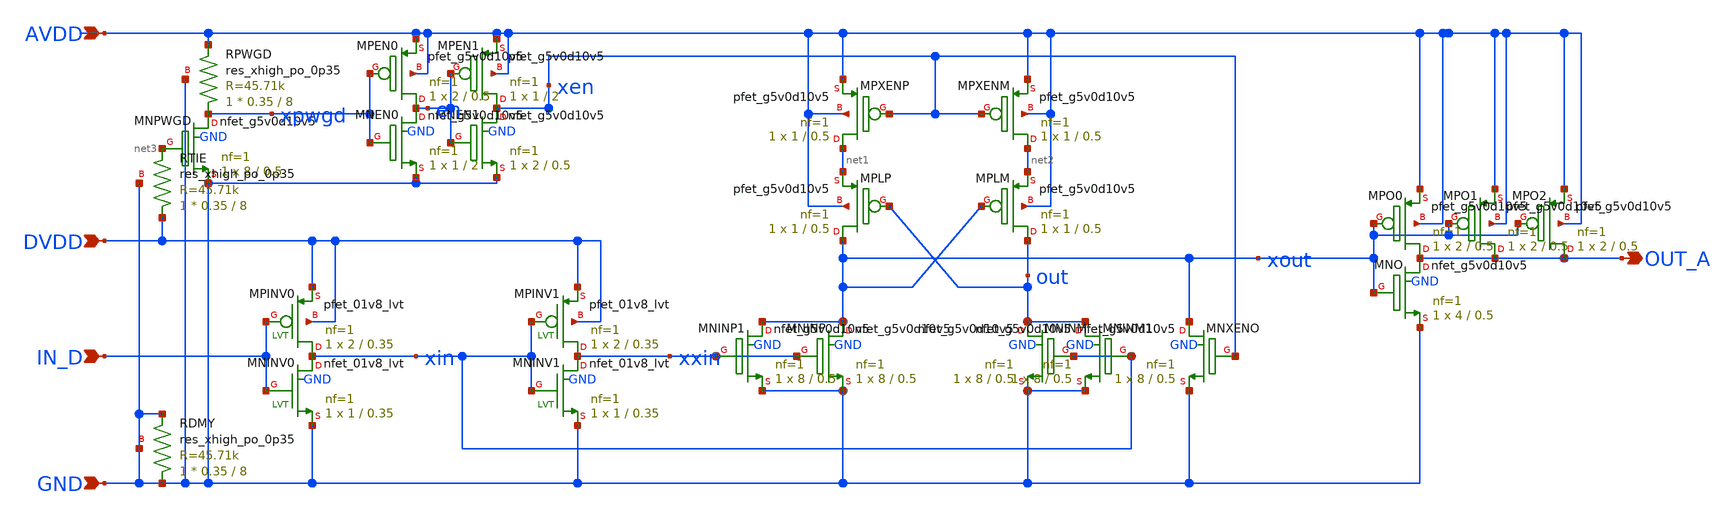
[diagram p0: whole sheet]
** sch_path: design/schematic/LVSHFTL2H_v1.sch
**.subckt LVSHFTL2H_v1 OUT_A AVDD DVDD GND IN_D
*.opin OUT_A
*.ipin AVDD
*.ipin DVDD
*.ipin GND
*.ipin IN_D
XMNINP xout xxin GND GND sky130_fd_pr__nfet_g5v0d10v5 L=0.5 W=8 nf=1 ad='int((nf+1)/2) * W/nf * 0.29'
+ as='int((nf+2)/2) * W/nf * 0.29' pd='2*int((nf+1)/2) * (W/nf + 0.29)' ps='2*int((nf+2)/2) * (W/nf + 0.29)'
+ nrd='0.29 / W' nrs='0.29 / W' sa=0 sb=0 sd=0 mult=1 m=1
XMNINM out xin GND GND sky130_fd_pr__nfet_g5v0d10v5 L=0.5 W=8 nf=1 ad='int((nf+1)/2) * W/nf * 0.29' as='int((nf+2)/2) * W/nf * 0.29'
+ pd='2*int((nf+1)/2) * (W/nf + 0.29)' ps='2*int((nf+2)/2) * (W/nf + 0.29)' nrd='0.29 / W' nrs='0.29 / W'
+ sa=0 sb=0 sd=0 mult=1 m=1
XMPLM out xout net2 AVDD sky130_fd_pr__pfet_g5v0d10v5 L=0.5 W=1 nf=1 ad='int((1 + 1)/2) * 1 / 1 * 0.29'
+ as='int((1 + 2)/2) * 1 / 1 * 0.29' pd='2*int((1 + 1)/2) * (1 / 1 + 0.29)' ps='2*int((1 + 2)/2) * (1 / 1 + 0.29)'
+ nrd='0.29 / 1 ' nrs='0.29 / 1 ' sa=0 sb=0 sd=0 mult=1 m=1
XMPLP xout out net1 AVDD sky130_fd_pr__pfet_g5v0d10v5 L=0.5 W=1 nf=1 ad='int((1 + 1)/2) * 1 / 1 * 0.29'
+ as='int((1 + 2)/2) * 1 / 1 * 0.29' pd='2*int((1 + 1)/2) * (1 / 1 + 0.29)' ps='2*int((1 + 2)/2) * (1 / 1 + 0.29)'
+ nrd='0.29 / 1 ' nrs='0.29 / 1 ' sa=0 sb=0 sd=0 mult=1 m=1
XMPXENM net2 xen AVDD AVDD sky130_fd_pr__pfet_g5v0d10v5 L=0.5 W=1 nf=1 ad='int((1 + 1)/2) * 1 / 1 * 0.29'
+ as='int((1 + 2)/2) * 1 / 1 * 0.29' pd='2*int((1 + 1)/2) * (1 / 1 + 0.29)' ps='2*int((1 + 2)/2) * (1 / 1 + 0.29)'
+ nrd='0.29 / 1 ' nrs='0.29 / 1 ' sa=0 sb=0 sd=0 mult=1 m=1
XMPXENP net1 xen AVDD AVDD sky130_fd_pr__pfet_g5v0d10v5 L=0.5 W=1 nf=1 ad='int((1 + 1)/2) * 1 / 1 * 0.29'
+ as='int((1 + 2)/2) * 1 / 1 * 0.29' pd='2*int((1 + 1)/2) * (1 / 1 + 0.29)' ps='2*int((1 + 2)/2) * (1 / 1 + 0.29)'
+ nrd='0.29 / 1 ' nrs='0.29 / 1 ' sa=0 sb=0 sd=0 mult=1 m=1
XMNINV0 xin IN_D GND GND sky130_fd_pr__nfet_01v8_lvt L=0.35 W=1 nf=1 ad='int((1 + 1)/2) * 1 / 1 * 0.29'
+ as='int((1 + 2)/2) * 1 / 1 * 0.29' pd='2*int((1 + 1)/2) * (1 / 1 + 0.29)' ps='2*int((1 + 2)/2) * (1 / 1 + 0.29)'
+ nrd='0.29 / 1 ' nrs='0.29 / 1 ' sa=0 sb=0 sd=0 mult=1 m=1
XMPINV0 xin IN_D DVDD DVDD sky130_fd_pr__pfet_01v8_lvt L=0.35 W=2 nf=1 ad='int((1 + 1)/2) * 2 / 1 * 0.29'
+ as='int((1 + 2)/2) * 2 / 1 * 0.29' pd='2*int((1 + 1)/2) * (2 / 1 + 0.29)' ps='2*int((1 + 2)/2) * (2 / 1 + 0.29)'
+ nrd='0.29 / 2 ' nrs='0.29 / 2 ' sa=0 sb=0 sd=0 mult=1 m=1
XMNXENO xout xen GND GND sky130_fd_pr__nfet_g5v0d10v5 L=0.5 W=8 nf=1 ad='int((nf+1)/2) * W/nf * 0.29'
+ as='int((nf+2)/2) * W/nf * 0.29' pd='2*int((nf+1)/2) * (W/nf + 0.29)' ps='2*int((nf+2)/2) * (W/nf + 0.29)'
+ nrd='0.29 / W' nrs='0.29 / W' sa=0 sb=0 sd=0 mult=1 m=1
XMNINP1 xout xxin GND GND sky130_fd_pr__nfet_g5v0d10v5 L=0.5 W=8 nf=1 ad='int((nf+1)/2) * W/nf * 0.29'
+ as='int((nf+2)/2) * W/nf * 0.29' pd='2*int((nf+1)/2) * (W/nf + 0.29)' ps='2*int((nf+2)/2) * (W/nf + 0.29)'
+ nrd='0.29 / W' nrs='0.29 / W' sa=0 sb=0 sd=0 mult=1 m=1
XMNINM1 out xin GND GND sky130_fd_pr__nfet_g5v0d10v5 L=0.5 W=8 nf=1 ad='int((nf+1)/2) * W/nf * 0.29'
+ as='int((nf+2)/2) * W/nf * 0.29' pd='2*int((nf+1)/2) * (W/nf + 0.29)' ps='2*int((nf+2)/2) * (W/nf + 0.29)'
+ nrd='0.29 / W' nrs='0.29 / W' sa=0 sb=0 sd=0 mult=1 m=1
XMNINV1 xxin xin GND GND sky130_fd_pr__nfet_01v8_lvt L=0.35 W=1 nf=1 ad='int((1 + 1)/2) * 1 / 1 * 0.29'
+ as='int((1 + 2)/2) * 1 / 1 * 0.29' pd='2*int((1 + 1)/2) * (1 / 1 + 0.29)' ps='2*int((1 + 2)/2) * (1 / 1 + 0.29)'
+ nrd='0.29 / 1 ' nrs='0.29 / 1 ' sa=0 sb=0 sd=0 mult=1 m=1
XMPINV1 xxin xin DVDD DVDD sky130_fd_pr__pfet_01v8_lvt L=0.35 W=2 nf=1 ad='int((1 + 1)/2) * 2 / 1 * 0.29'
+ as='int((1 + 2)/2) * 2 / 1 * 0.29' pd='2*int((1 + 1)/2) * (2 / 1 + 0.29)' ps='2*int((1 + 2)/2) * (2 / 1 + 0.29)'
+ nrd='0.29 / 2 ' nrs='0.29 / 2 ' sa=0 sb=0 sd=0 mult=1 m=1
XRPWGD xpwgd AVDD GND sky130_fd_pr__res_xhigh_po_0p35 L=8 mult=1 m=1
XMNPWGD xpwgd net3 GND GND sky130_fd_pr__nfet_g5v0d10v5 L=0.5 W=8 nf=1 ad='int((nf+1)/2) * W/nf * 0.29'
+ as='int((nf+2)/2) * W/nf * 0.29' pd='2*int((nf+1)/2) * (W/nf + 0.29)' ps='2*int((nf+2)/2) * (W/nf + 0.29)'
+ nrd='0.29 / W' nrs='0.29 / W' sa=0 sb=0 sd=0 mult=1 m=1
XMPO0 OUT_A xout AVDD AVDD sky130_fd_pr__pfet_g5v0d10v5 L=0.5 W=2 nf=1 ad='int((1 + 1)/2) * 2 / 1 * 0.29'
+ as='int((1 + 2)/2) * 2 / 1 * 0.29' pd='2*int((1 + 1)/2) * (2 / 1 + 0.29)' ps='2*int((1 + 2)/2) * (2 / 1 + 0.29)'
+ nrd='0.29 / 2 ' nrs='0.29 / 2 ' sa=0 sb=0 sd=0 mult=1 m=1
XMNO OUT_A xout GND GND sky130_fd_pr__nfet_g5v0d10v5 L=0.5 W=4 nf=1 ad='int((nf+1)/2) * W/nf * 0.29'
+ as='int((nf+2)/2) * W/nf * 0.29' pd='2*int((nf+1)/2) * (W/nf + 0.29)' ps='2*int((nf+2)/2) * (W/nf + 0.29)'
+ nrd='0.29 / W' nrs='0.29 / W' sa=0 sb=0 sd=0 mult=1 m=1
XMNEN0 en xpwgd GND GND sky130_fd_pr__nfet_g5v0d10v5 L=2 W=1 nf=1 ad='int((nf+1)/2) * W/nf * 0.29' as='int((nf+2)/2) * W/nf * 0.29'
+ pd='2*int((nf+1)/2) * (W/nf + 0.29)' ps='2*int((nf+2)/2) * (W/nf + 0.29)' nrd='0.29 / W' nrs='0.29 / W'
+ sa=0 sb=0 sd=0 mult=1 m=1
XMPEN0 en xpwgd AVDD AVDD sky130_fd_pr__pfet_g5v0d10v5 L=0.5 W=2 nf=1 ad='int((1 + 1)/2) * 2 / 1 * 0.29'
+ as='int((1 + 2)/2) * 2 / 1 * 0.29' pd='2*int((1 + 1)/2) * (2 / 1 + 0.29)' ps='2*int((1 + 2)/2) * (2 / 1 + 0.29)'
+ nrd='0.29 / 2 ' nrs='0.29 / 2 ' sa=0 sb=0 sd=0 mult=1 m=1
XMPEN1 xen en AVDD AVDD sky130_fd_pr__pfet_g5v0d10v5 L=2 W=1 nf=1 ad='int((1 + 1)/2) * 1 / 1 * 0.29'
+ as='int((1 + 2)/2) * 1 / 1 * 0.29' pd='2*int((1 + 1)/2) * (1 / 1 + 0.29)' ps='2*int((1 + 2)/2) * (1 / 1 + 0.29)'
+ nrd='0.29 / 1 ' nrs='0.29 / 1 ' sa=0 sb=0 sd=0 mult=1 m=1
XMNEN1 xen en GND GND sky130_fd_pr__nfet_g5v0d10v5 L=0.5 W=2 nf=1 ad='int((nf+1)/2) * W/nf * 0.29' as='int((nf+2)/2) * W/nf * 0.29'
+ pd='2*int((nf+1)/2) * (W/nf + 0.29)' ps='2*int((nf+2)/2) * (W/nf + 0.29)' nrd='0.29 / W' nrs='0.29 / W'
+ sa=0 sb=0 sd=0 mult=1 m=1
XMPO1 OUT_A xout AVDD AVDD sky130_fd_pr__pfet_g5v0d10v5 L=0.5 W=2 nf=1 ad='int((1 + 1)/2) * 2 / 1 * 0.29'
+ as='int((1 + 2)/2) * 2 / 1 * 0.29' pd='2*int((1 + 1)/2) * (2 / 1 + 0.29)' ps='2*int((1 + 2)/2) * (2 / 1 + 0.29)'
+ nrd='0.29 / 2 ' nrs='0.29 / 2 ' sa=0 sb=0 sd=0 mult=1 m=1
XMPO2 OUT_A xout AVDD AVDD sky130_fd_pr__pfet_g5v0d10v5 L=0.5 W=2 nf=1 ad='int((1 + 1)/2) * 2 / 1 * 0.29'
+ as='int((1 + 2)/2) * 2 / 1 * 0.29' pd='2*int((1 + 1)/2) * (2 / 1 + 0.29)' ps='2*int((1 + 2)/2) * (2 / 1 + 0.29)'
+ nrd='0.29 / 2 ' nrs='0.29 / 2 ' sa=0 sb=0 sd=0 mult=1 m=1
XRTIE DVDD net3 GND sky130_fd_pr__res_xhigh_po_0p35 L=8 mult=1 m=1
XRDMY GND GND GND sky130_fd_pr__res_xhigh_po_0p35 L=8 mult=1 m=1
**.ends
.end
